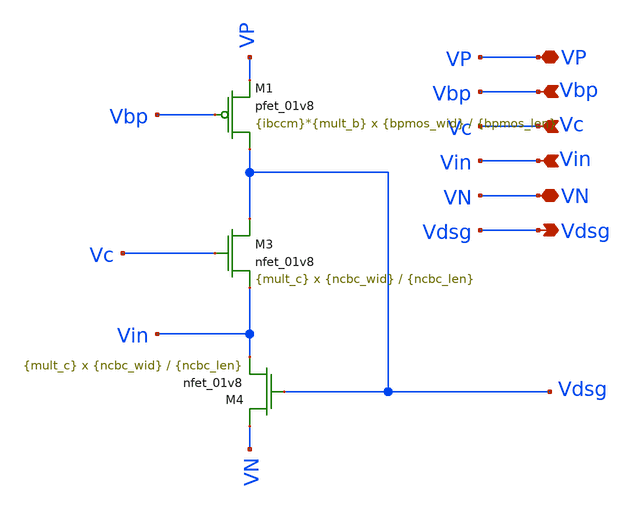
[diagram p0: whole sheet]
** sch_path: Circuits, Symbols, Extras/fvf.sch
**.subckt fvf VP Vbp Vc Vin VN Vdsg
*.iopin VP
*.ipin Vbp
*.ipin Vc
*.ipin Vin
*.iopin VN
*.opin Vdsg
XM3 Vdsg Vc Vin VN sky130_fd_pr__nfet_01v8 L={ncbc_len} W={ncbc_wid} nf=1 ad='int((nf+1)/2) * W/nf * 0.29'
+ as='int((nf+2)/2) * W/nf * 0.29' pd='2*int((nf+1)/2) * (W/nf + 0.29)' ps='2*int((nf+2)/2) * (W/nf + 0.29)'
+ nrd='0.29 / W' nrs='0.29 / W' sa=0 sb=0 sd=0 mult={mult_c} m={mult_c}
XM4 VN Vdsg Vin VN sky130_fd_pr__nfet_01v8 L={ncbc_len} W={ncbc_wid} nf=1 ad='int((nf+1)/2) * W/nf * 0.29'
+ as='int((nf+2)/2) * W/nf * 0.29' pd='2*int((nf+1)/2) * (W/nf + 0.29)' ps='2*int((nf+2)/2) * (W/nf + 0.29)'
+ nrd='0.29 / W' nrs='0.29 / W' sa=0 sb=0 sd=0 mult={mult_c} m={mult_c}
XM1 Vdsg Vbp VP VP sky130_fd_pr__pfet_01v8 L={bpmos_len} W={bpmos_wid} nf=1 ad='int((nf+1)/2) * W/nf * 0.29'
+ as='int((nf+2)/2) * W/nf * 0.29' pd='2*int((nf+1)/2) * (W/nf + 0.29)' ps='2*int((nf+2)/2) * (W/nf + 0.29)'
+ nrd='0.29 / W' nrs='0.29 / W' sa=0 sb=0 sd=0 mult={ibccm}*{mult_b} m={ibccm}*{mult_b}
**.ends
.end
